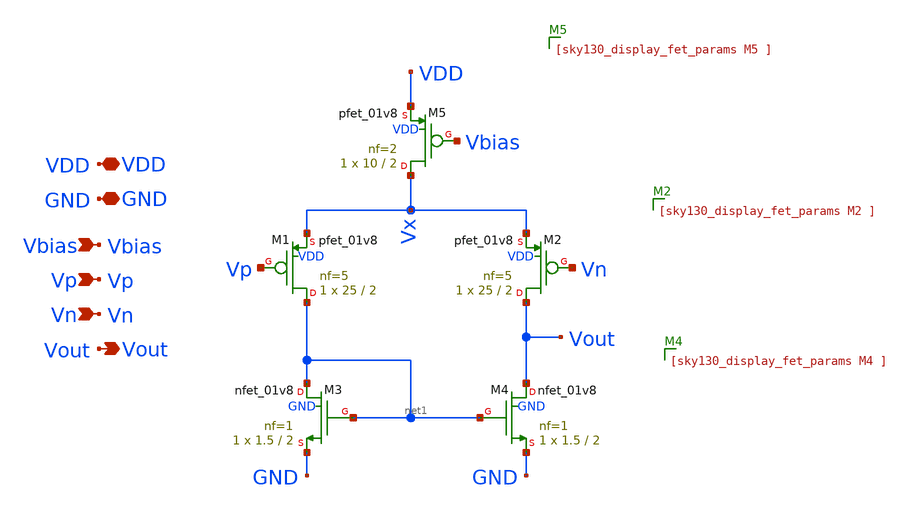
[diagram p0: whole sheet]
** sch_path: sch/cascode/ota_p.sch
**.subckt ota_p Vbias Vout VDD GND Vp Vn
*.ipin Vbias
*.opin Vout
*.iopin VDD
*.iopin GND
*.ipin Vp
*.ipin Vn
XM1 net1 Vp Vx VDD sky130_fd_pr__pfet_01v8 L=2 W=25 nf=5 ad='int((5 + 1)/2) * 25 / 5 * 0.29' as='int((5 + 2)/2) * 25 / 5 * 0.29'
+ pd='2*int((5 + 1)/2) * (25 / 5 + 0.29)' ps='2*int((5 + 2)/2) * (25 / 5 + 0.29)' nrd='0.29 / 25 ' nrs='0.29 / 25 '
+ sa=0 sb=0 sd=0 mult=1 m=1
XM2 Vout Vn Vx VDD sky130_fd_pr__pfet_01v8 L=2 W=25 nf=5 ad='int((5 + 1)/2) * 25 / 5 * 0.29' as='int((5 + 2)/2) * 25 / 5 * 0.29'
+ pd='2*int((5 + 1)/2) * (25 / 5 + 0.29)' ps='2*int((5 + 2)/2) * (25 / 5 + 0.29)' nrd='0.29 / 25 ' nrs='0.29 / 25 '
+ sa=0 sb=0 sd=0 mult=1 m=1
XM3 net1 net1 GND GND sky130_fd_pr__nfet_01v8 L=2 W=1.5 nf=1 ad='int((1 + 1)/2) * 1.5 / 1 * 0.29' as='int((1 + 2)/2) * 1.5 / 1 * 0.29'
+ pd='2*int((1 + 1)/2) * (1.5 / 1 + 0.29)' ps='2*int((1 + 2)/2) * (1.5 / 1 + 0.29)' nrd='0.29 / 1.5 ' nrs='0.29 / 1.5 '
+ sa=0 sb=0 sd=0 mult=1 m=1
XM4 Vout net1 GND GND sky130_fd_pr__nfet_01v8 L=2 W=1.5 nf=1 ad='int((1 + 1)/2) * 1.5 / 1 * 0.29' as='int((1 + 2)/2) * 1.5 / 1 * 0.29'
+ pd='2*int((1 + 1)/2) * (1.5 / 1 + 0.29)' ps='2*int((1 + 2)/2) * (1.5 / 1 + 0.29)' nrd='0.29 / 1.5 ' nrs='0.29 / 1.5 '
+ sa=0 sb=0 sd=0 mult=1 m=1
XM5 Vx Vbias VDD VDD sky130_fd_pr__pfet_01v8 L=2 W=10 nf=2 ad='int((2 + 1)/2) * 10 / 2 * 0.29' as='int((2 + 2)/2) * 10 / 2 * 0.29'
+ pd='2*int((2 + 1)/2) * (10 / 2 + 0.29)' ps='2*int((2 + 2)/2) * (10 / 2 + 0.29)' nrd='0.29 / 10 ' nrs='0.29 / 10 '
+ sa=0 sb=0 sd=0 mult=1 m=1
**.ends
.end
